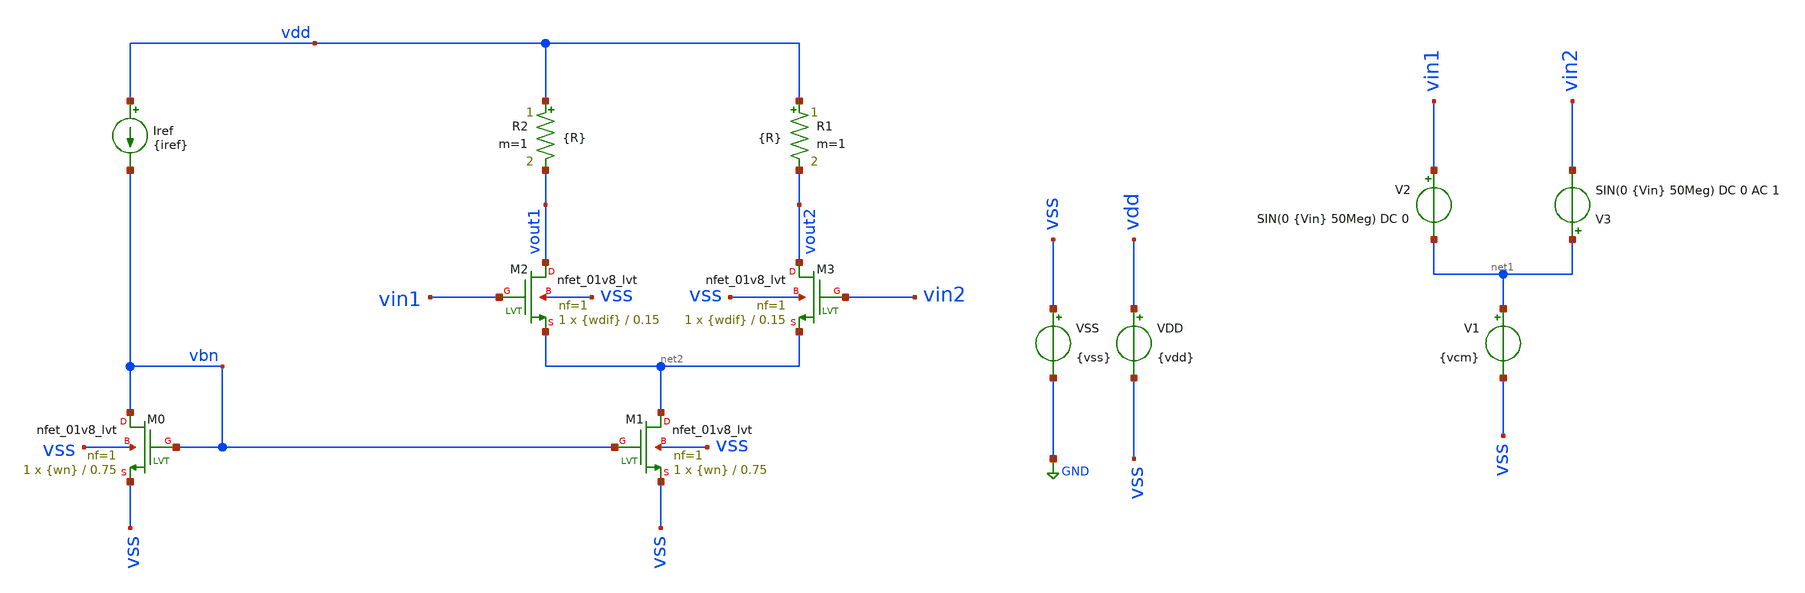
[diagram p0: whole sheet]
** sch_path: Tp3/Simulaciones/tp3_1a.sch
**.subckt tp3_1a
Iref vdd vbn {iref}
VSS vss GND {vss}
VDD vdd vss {vdd}
V1 net1 vss {vcm}
XM1 net2 vbn vss vss sky130_fd_pr__nfet_01v8_lvt L=0.75 W={wn} nf=1 ad='int((nf+1)/2) * W/nf * 0.29'
+ as='int((nf+2)/2) * W/nf * 0.29' pd='2*int((nf+1)/2) * (W/nf + 0.29)' ps='2*int((nf+2)/2) * (W/nf + 0.29)'
+ nrd='0.29 / W' nrs='0.29 / W' sa=0 sb=0 sd=0 mult=1 m=1
XM0 vbn vbn vss vss sky130_fd_pr__nfet_01v8_lvt L=0.75 W={wn} nf=1 ad='int((nf+1)/2) * W/nf * 0.29' as='int((nf+2)/2) * W/nf * 0.29'
+ pd='2*int((nf+1)/2) * (W/nf + 0.29)' ps='2*int((nf+2)/2) * (W/nf + 0.29)' nrd='0.29 / W' nrs='0.29 / W'
+ sa=0 sb=0 sd=0 mult=1 m=1
XM2 vout1 vin1 net2 vss sky130_fd_pr__nfet_01v8_lvt L=0.15 W={wdif} nf=1 ad='int((nf+1)/2) * W/nf * 0.29'
+ as='int((nf+2)/2) * W/nf * 0.29' pd='2*int((nf+1)/2) * (W/nf + 0.29)' ps='2*int((nf+2)/2) * (W/nf + 0.29)'
+ nrd='0.29 / W' nrs='0.29 / W' sa=0 sb=0 sd=0 mult=1 m=1
R2 vdd vout1 {R} m=1
XM3 vout2 vin2 net2 vss sky130_fd_pr__nfet_01v8_lvt L=0.15 W={wdif} nf=1 ad='int((nf+1)/2) * W/nf * 0.29'
+ as='int((nf+2)/2) * W/nf * 0.29' pd='2*int((nf+1)/2) * (W/nf + 0.29)' ps='2*int((nf+2)/2) * (W/nf + 0.29)'
+ nrd='0.29 / W' nrs='0.29 / W' sa=0 sb=0 sd=0 mult=1 m=1
R1 vdd vout2 {R} m=1
V2 vin1 net1 SIN(0 {Vin} 50Meg) DC 0
V3 net1 vin2 SIN(0 {Vin} 50Meg) DC 0 AC 1
**** begin user architecture code



* Parameters
.param vdd = 1.8
.param vss = 0
.param vcm = 1.2
.param iref = 25u
.param R = 48K
.param Vin = 70m
.param wn = 21
.param wdif = 4

.options TEMP = 65.0

* Models
.lib ~/skywater/skywater-pdk/libraries/sky130_fd_pr_ngspice/latest/models/corners/sky130.lib TT

* Data to save
.save all  @M.XM0.msky130_fd_pr__nfet_01v8_lvt[vth]  @M.XM1.msky130_fd_pr__nfet_01v8_lvt[id]  @M.XM1.msky130_fd_pr__nfet_01v8_lvt[vth]  @M.XM2.msky130_fd_pr__nfet_01v8_lvt[vdsat]  @M.XM2.msky130_fd_pr__nfet_01v8_lvt[gds]  @M.XM2.msky130_fd_pr__nfet_01v8_lvt[gm]  @M.XM2.msky130_fd_pr__nfet_01v8_lvt[id]  @M.XM2.msky130_fd_pr__nfet_01v8_lvt[vth]  @M.XM3.msky130_fd_pr__nfet_01v8_lvt[vdsat]  @M.XM3.msky130_fd_pr__nfet_01v8_lvt[gds]  @M.XM3.msky130_fd_pr__nfet_01v8_lvt[gm]  @M.XM3.msky130_fd_pr__nfet_01v8_lvt[id]  @M.XM3.msky130_fd_pr__nfet_01v8_lvt[vth]

* Simulation
.control
  *let wi = 1.5
  *let wf = 4.5
  *let wstep = 0.15

  *dowhile wi <= wf
    *print @M.XM0.msky130_fd_pr__nfet_01v8_lvt[w]
    *alter @M.XM0.msky130_fd_pr__nfet_01v8_lvt[w] = wi
    *alter @M.XM1.msky130_fd_pr__nfet_01v8_lvt[w] = wi
    *let wi = wi + wstep
    *op
    *print @M.XM0.msky130_fd_pr__nfet_01v8_lvt[w]
    *print @M.XM0.msky130_fd_pr__nfet_01v8_lvt[vth]
    *print @M.XM1.msky130_fd_pr__nfet_01v8_lvt[w]
    *print @M.XM1.msky130_fd_pr__nfet_01v8_lvt[id]
    *print @M.XM1.msky130_fd_pr__nfet_01v8_lvt[vth]
    *print @M.XM2.msky130_fd_pr__nfet_01v8_lvt[w]
    *print @M.XM2.msky130_fd_pr__nfet_01v8_lvt[vdsat]
    *print @M.XM2.msky130_fd_pr__nfet_01v8_lvt[gds]
    *print @M.XM2.msky130_fd_pr__nfet_01v8_lvt[gm]
    *print @M.XM2.msky130_fd_pr__nfet_01v8_lvt[id]
    *print @M.XM2.msky130_fd_pr__nfet_01v8_lvt[vth]
    *print @M.XM3.msky130_fd_pr__nfet_01v8_lvt[w]
    *print @M.XM3.msky130_fd_pr__nfet_01v8_lvt[vdsat]
    *print @M.XM3.msky130_fd_pr__nfet_01v8_lvt[gds]
    *print @M.XM3.msky130_fd_pr__nfet_01v8_lvt[gm]
    *print @M.XM3.msky130_fd_pr__nfet_01v8_lvt[id]
    *print @M.XM3.msky130_fd_pr__nfet_01v8_lvt[vth]
    *save all
  *end
  *write tp3_1a_datos.raw

  ac dec 100 10k 100G
  setplot ac1
  plot vdb(vout2) {vp(vout2)*180/PI}
  write tp3_1a_ac.raw

  reset
  tran 0.01n 100n
  plot v(vin2) v(vout2)
  write tp3_1a_tran.raw

  reset
  op
  save all
  print all
  unset filetype
  write tp3_1a.raw
.endc

.end


**** end user architecture code
**.ends
.GLOBAL GND
.end
